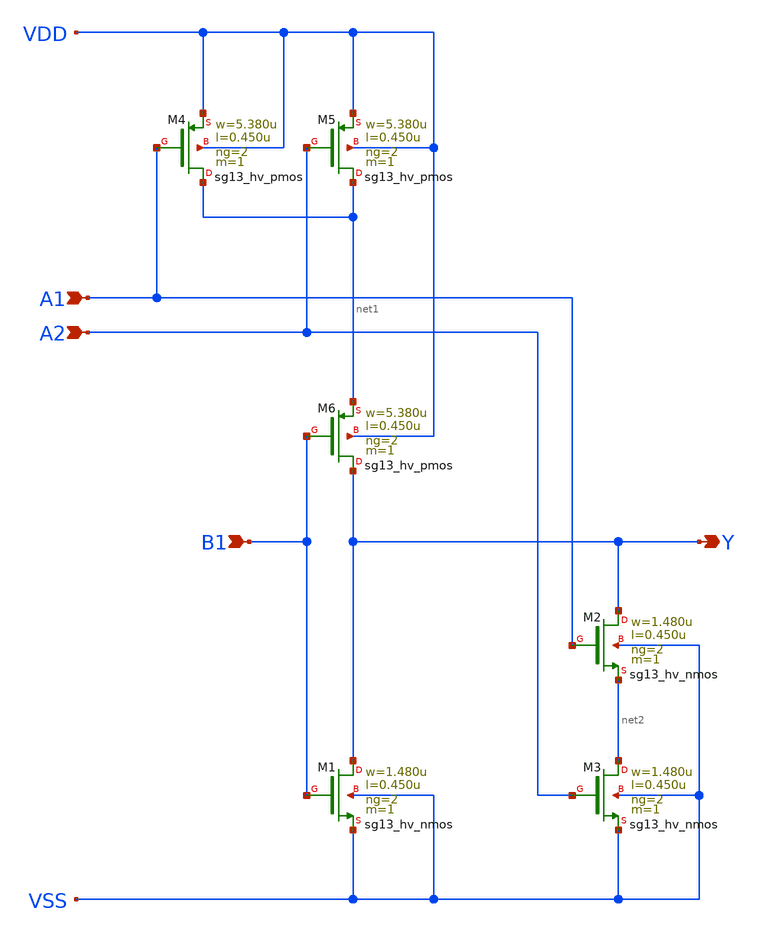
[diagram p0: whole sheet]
** sch_path: ihp-sg13g2/libs.ref/sg13g2_stdcell_hv/sch/xschem/sg13g2_hv_a21oi_2.sch
* Copyright 2023 IHP PDK Authors
* Licensed under the Apache License, Version 2.0 (the "License");
* you may not use this file except in compliance with the License.
* You may obtain a copy of the License at
* https://www.apache.org/licenses/LICENSE-2.0
* Unless required by applicable law or agreed to in writing, software
* distributed under the License is distributed on an "AS IS" BASIS,
* WITHOUT WARRANTIES OR CONDITIONS OF ANY KIND, either express or implied.
* See the License for the specific language governing permissions and
* limitations under the License.
**.subckt sg13g2_hv_a21oi_2 A1 A2 B1 Y
*.ipin A1
*.ipin A2
*.ipin B1
*.opin Y
XM1 Y B1 VSS VSS sg13_hv_nmos w=1.480u l=0.450u ng=2 m=1 mm_ok=1
XM2 Y A1 net2 VSS sg13_hv_nmos w=1.480u l=0.450u ng=2 m=1 mm_ok=1
XM3 net2 A2 VSS VSS sg13_hv_nmos w=1.480u l=0.450u ng=2 m=1 mm_ok=1
XM4 net1 A1 VDD VDD sg13_hv_pmos w=5.380u l=0.450u ng=2 m=1 mm_ok=1
XM5 net1 A2 VDD VDD sg13_hv_pmos w=5.380u l=0.450u ng=2 m=1 mm_ok=1
XM6 Y B1 net1 VDD sg13_hv_pmos w=5.380u l=0.450u ng=2 m=1 mm_ok=1
**.ends
.end
